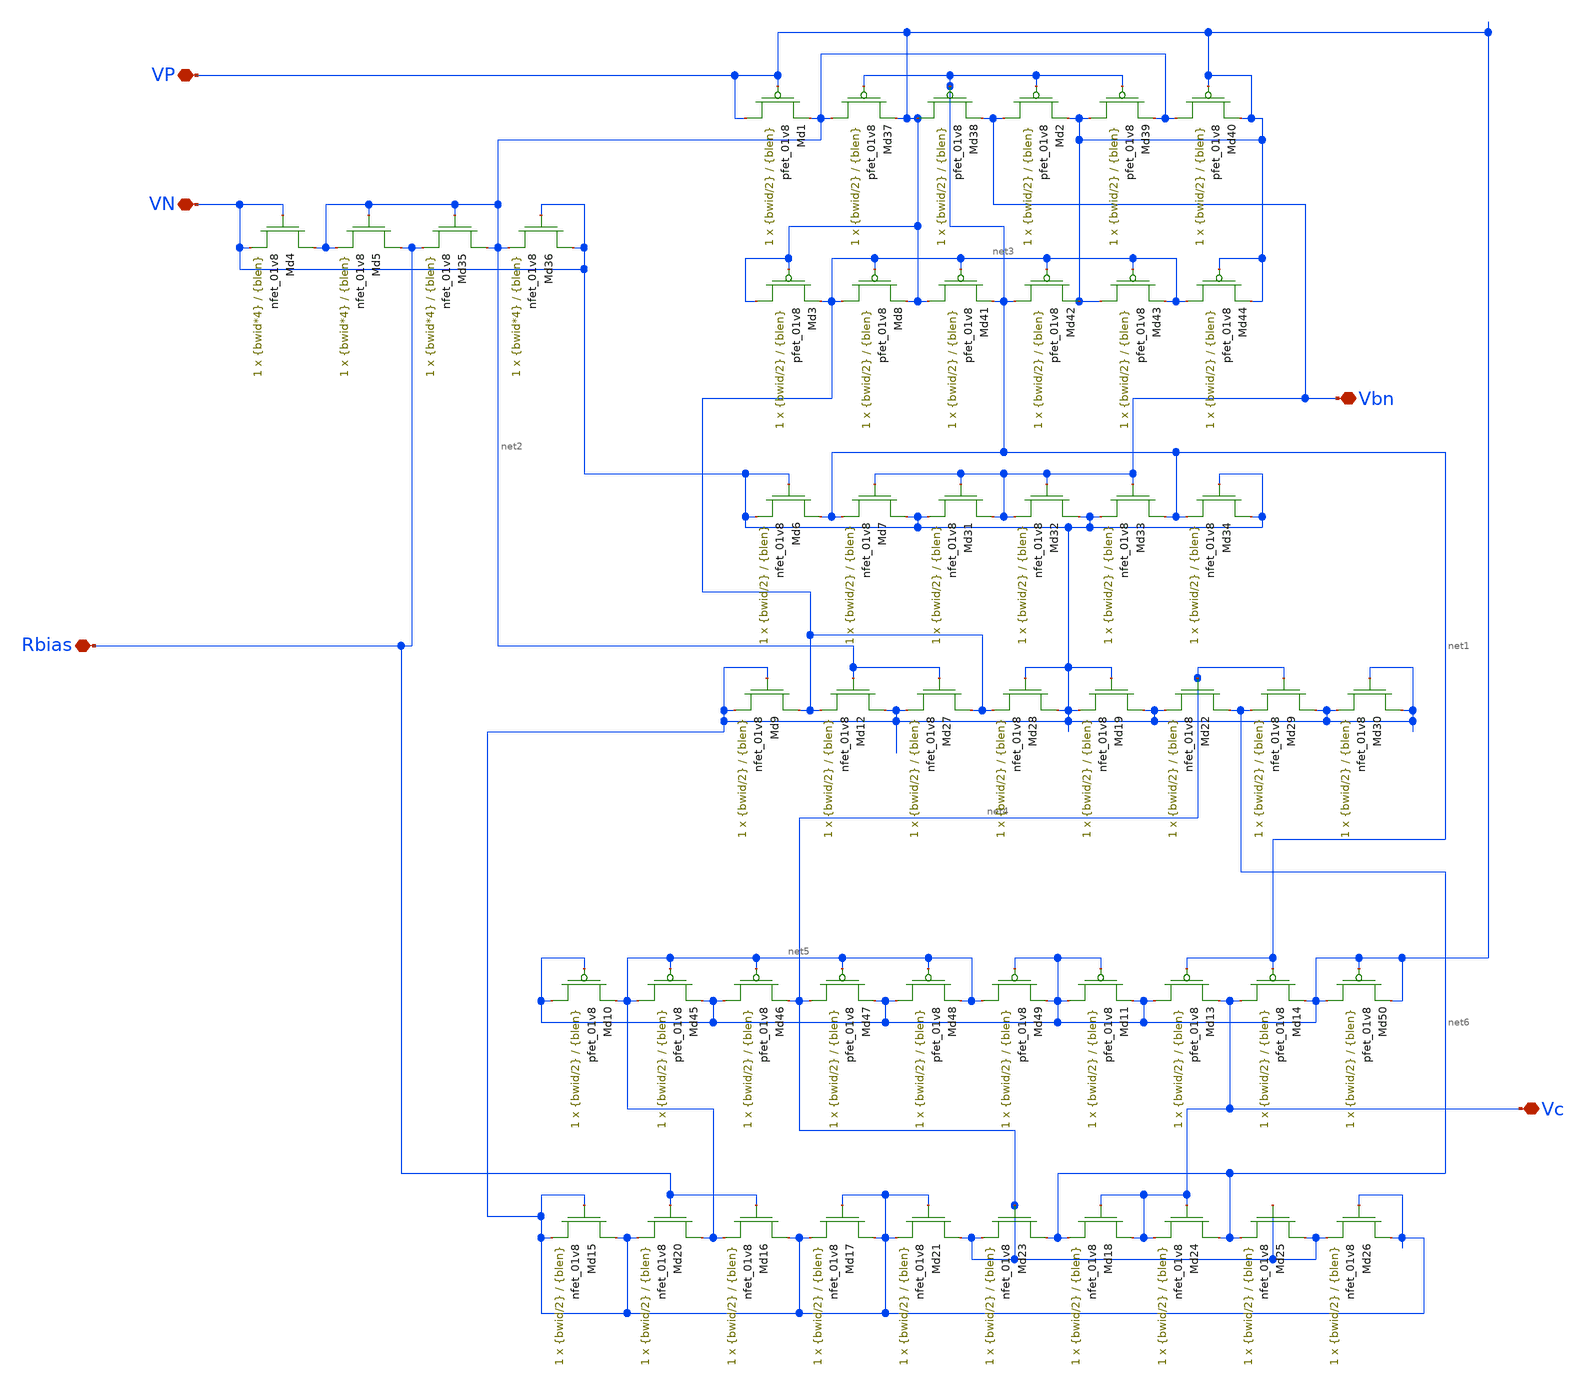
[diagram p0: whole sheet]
** sch_path: design-files/improved/biasgen-m2.sch
**.subckt biasgen-m2 Rbias Vbn Vc VP VN
*.iopin Rbias
*.iopin Vbn
*.iopin Vc
*.iopin VP
*.iopin VN
XMd1 VP VP net2 VDD sky130_fd_pr__pfet_01v8 L={blen} W={bwid/2} nf=1 ad='int((nf+1)/2) * W/nf * 0.29'
+ as='int((nf+2)/2) * W/nf * 0.29' pd='2*int((nf+1)/2) * (W/nf + 0.29)' ps='2*int((nf+2)/2) * (W/nf + 0.29)'
+ nrd='0.29 / W' nrs='0.29 / W' sa=0 sb=0 sd=0 mult=1 m=1
XMd15 VN VN VN GND sky130_fd_pr__nfet_01v8 L={blen} W={bwid/2} nf=1 ad='int((nf+1)/2) * W/nf * 0.29'
+ as='int((nf+2)/2) * W/nf * 0.29' pd='2*int((nf+1)/2) * (W/nf + 0.29)' ps='2*int((nf+2)/2) * (W/nf + 0.29)'
+ nrd='0.29 / W' nrs='0.29 / W' sa=0 sb=0 sd=0 mult=1 m=1
XMd20 net5 Rbias VN GND sky130_fd_pr__nfet_01v8 L={blen} W={bwid/2} nf=1 ad='int((nf+1)/2) * W/nf * 0.29'
+ as='int((nf+2)/2) * W/nf * 0.29' pd='2*int((nf+1)/2) * (W/nf + 0.29)' ps='2*int((nf+2)/2) * (W/nf + 0.29)'
+ nrd='0.29 / W' nrs='0.29 / W' sa=0 sb=0 sd=0 mult=1 m=1
XMd16 VN Rbias net5 GND sky130_fd_pr__nfet_01v8 L={blen} W={bwid/2} nf=1 ad='int((nf+1)/2) * W/nf * 0.29'
+ as='int((nf+2)/2) * W/nf * 0.29' pd='2*int((nf+1)/2) * (W/nf + 0.29)' ps='2*int((nf+2)/2) * (W/nf + 0.29)'
+ nrd='0.29 / W' nrs='0.29 / W' sa=0 sb=0 sd=0 mult=1 m=1
XMd17 VN VN VN GND sky130_fd_pr__nfet_01v8 L={blen} W={bwid/2} nf=1 ad='int((nf+1)/2) * W/nf * 0.29'
+ as='int((nf+2)/2) * W/nf * 0.29' pd='2*int((nf+1)/2) * (W/nf + 0.29)' ps='2*int((nf+2)/2) * (W/nf + 0.29)'
+ nrd='0.29 / W' nrs='0.29 / W' sa=0 sb=0 sd=0 mult=1 m=1
XMd21 net4 VN VN GND sky130_fd_pr__nfet_01v8 L={blen} W={bwid/2} nf=1 ad='int((nf+1)/2) * W/nf * 0.29'
+ as='int((nf+2)/2) * W/nf * 0.29' pd='2*int((nf+1)/2) * (W/nf + 0.29)' ps='2*int((nf+2)/2) * (W/nf + 0.29)'
+ nrd='0.29 / W' nrs='0.29 / W' sa=0 sb=0 sd=0 mult=1 m=1
XMd23 net6 net4 net4 GND sky130_fd_pr__nfet_01v8 L={blen} W={bwid/2} nf=1 ad='int((nf+1)/2) * W/nf * 0.29'
+ as='int((nf+2)/2) * W/nf * 0.29' pd='2*int((nf+1)/2) * (W/nf + 0.29)' ps='2*int((nf+2)/2) * (W/nf + 0.29)'
+ nrd='0.29 / W' nrs='0.29 / W' sa=0 sb=0 sd=0 mult=1 m=1
XMd18 Vc Vc net6 GND sky130_fd_pr__nfet_01v8 L={blen} W={bwid/2} nf=1 ad='int((nf+1)/2) * W/nf * 0.29'
+ as='int((nf+2)/2) * W/nf * 0.29' pd='2*int((nf+1)/2) * (W/nf + 0.29)' ps='2*int((nf+2)/2) * (W/nf + 0.29)'
+ nrd='0.29 / W' nrs='0.29 / W' sa=0 sb=0 sd=0 mult=1 m=1
XMd24 net6 Vc Vc GND sky130_fd_pr__nfet_01v8 L={blen} W={bwid/2} nf=1 ad='int((nf+1)/2) * W/nf * 0.29'
+ as='int((nf+2)/2) * W/nf * 0.29' pd='2*int((nf+1)/2) * (W/nf + 0.29)' ps='2*int((nf+2)/2) * (W/nf + 0.29)'
+ nrd='0.29 / W' nrs='0.29 / W' sa=0 sb=0 sd=0 mult=1 m=1
XMd25 net4 net4 net6 GND sky130_fd_pr__nfet_01v8 L={blen} W={bwid/2} nf=1 ad='int((nf+1)/2) * W/nf * 0.29'
+ as='int((nf+2)/2) * W/nf * 0.29' pd='2*int((nf+1)/2) * (W/nf + 0.29)' ps='2*int((nf+2)/2) * (W/nf + 0.29)'
+ nrd='0.29 / W' nrs='0.29 / W' sa=0 sb=0 sd=0 mult=1 m=1
XMd26 VN VN net4 GND sky130_fd_pr__nfet_01v8 L={blen} W={bwid/2} nf=1 ad='int((nf+1)/2) * W/nf * 0.29'
+ as='int((nf+2)/2) * W/nf * 0.29' pd='2*int((nf+1)/2) * (W/nf + 0.29)' ps='2*int((nf+2)/2) * (W/nf + 0.29)'
+ nrd='0.29 / W' nrs='0.29 / W' sa=0 sb=0 sd=0 mult=1 m=1
XMd9 net3 VN VN GND sky130_fd_pr__nfet_01v8 L={blen} W={bwid/2} nf=1 ad='int((nf+1)/2) * W/nf * 0.29'
+ as='int((nf+2)/2) * W/nf * 0.29' pd='2*int((nf+1)/2) * (W/nf + 0.29)' ps='2*int((nf+2)/2) * (W/nf + 0.29)'
+ nrd='0.29 / W' nrs='0.29 / W' sa=0 sb=0 sd=0 mult=1 m=1
XMd12 VN net2 net3 GND sky130_fd_pr__nfet_01v8 L={blen} W={bwid/2} nf=1 ad='int((nf+1)/2) * W/nf * 0.29'
+ as='int((nf+2)/2) * W/nf * 0.29' pd='2*int((nf+1)/2) * (W/nf + 0.29)' ps='2*int((nf+2)/2) * (W/nf + 0.29)'
+ nrd='0.29 / W' nrs='0.29 / W' sa=0 sb=0 sd=0 mult=1 m=1
XMd27 net3 net2 VN GND sky130_fd_pr__nfet_01v8 L={blen} W={bwid/2} nf=1 ad='int((nf+1)/2) * W/nf * 0.29'
+ as='int((nf+2)/2) * W/nf * 0.29' pd='2*int((nf+1)/2) * (W/nf + 0.29)' ps='2*int((nf+2)/2) * (W/nf + 0.29)'
+ nrd='0.29 / W' nrs='0.29 / W' sa=0 sb=0 sd=0 mult=1 m=1
XMd28 VN VN net3 GND sky130_fd_pr__nfet_01v8 L={blen} W={bwid/2} nf=1 ad='int((nf+1)/2) * W/nf * 0.29'
+ as='int((nf+2)/2) * W/nf * 0.29' pd='2*int((nf+1)/2) * (W/nf + 0.29)' ps='2*int((nf+2)/2) * (W/nf + 0.29)'
+ nrd='0.29 / W' nrs='0.29 / W' sa=0 sb=0 sd=0 mult=1 m=1
XMd19 VN VN VN GND sky130_fd_pr__nfet_01v8 L={blen} W={bwid/2} nf=1 ad='int((nf+1)/2) * W/nf * 0.29'
+ as='int((nf+2)/2) * W/nf * 0.29' pd='2*int((nf+1)/2) * (W/nf + 0.29)' ps='2*int((nf+2)/2) * (W/nf + 0.29)'
+ nrd='0.29 / W' nrs='0.29 / W' sa=0 sb=0 sd=0 mult=1 m=1
XMd22 net6 net4 VN GND sky130_fd_pr__nfet_01v8 L={blen} W={bwid/2} nf=1 ad='int((nf+1)/2) * W/nf * 0.29'
+ as='int((nf+2)/2) * W/nf * 0.29' pd='2*int((nf+1)/2) * (W/nf + 0.29)' ps='2*int((nf+2)/2) * (W/nf + 0.29)'
+ nrd='0.29 / W' nrs='0.29 / W' sa=0 sb=0 sd=0 mult=1 m=1
XMd29 VN net4 net6 GND sky130_fd_pr__nfet_01v8 L={blen} W={bwid/2} nf=1 ad='int((nf+1)/2) * W/nf * 0.29'
+ as='int((nf+2)/2) * W/nf * 0.29' pd='2*int((nf+1)/2) * (W/nf + 0.29)' ps='2*int((nf+2)/2) * (W/nf + 0.29)'
+ nrd='0.29 / W' nrs='0.29 / W' sa=0 sb=0 sd=0 mult=1 m=1
XMd30 VN VN VN GND sky130_fd_pr__nfet_01v8 L={blen} W={bwid/2} nf=1 ad='int((nf+1)/2) * W/nf * 0.29'
+ as='int((nf+2)/2) * W/nf * 0.29' pd='2*int((nf+1)/2) * (W/nf + 0.29)' ps='2*int((nf+2)/2) * (W/nf + 0.29)'
+ nrd='0.29 / W' nrs='0.29 / W' sa=0 sb=0 sd=0 mult=1 m=1
XMd6 net1 VN VN GND sky130_fd_pr__nfet_01v8 L={blen} W={bwid/2} nf=1 ad='int((nf+1)/2) * W/nf * 0.29'
+ as='int((nf+2)/2) * W/nf * 0.29' pd='2*int((nf+1)/2) * (W/nf + 0.29)' ps='2*int((nf+2)/2) * (W/nf + 0.29)'
+ nrd='0.29 / W' nrs='0.29 / W' sa=0 sb=0 sd=0 mult=1 m=1
XMd7 VN Vbn net1 GND sky130_fd_pr__nfet_01v8 L={blen} W={bwid/2} nf=1 ad='int((nf+1)/2) * W/nf * 0.29'
+ as='int((nf+2)/2) * W/nf * 0.29' pd='2*int((nf+1)/2) * (W/nf + 0.29)' ps='2*int((nf+2)/2) * (W/nf + 0.29)'
+ nrd='0.29 / W' nrs='0.29 / W' sa=0 sb=0 sd=0 mult=1 m=1
XMd31 Vbn Vbn VN GND sky130_fd_pr__nfet_01v8 L={blen} W={bwid/2} nf=1 ad='int((nf+1)/2) * W/nf * 0.29'
+ as='int((nf+2)/2) * W/nf * 0.29' pd='2*int((nf+1)/2) * (W/nf + 0.29)' ps='2*int((nf+2)/2) * (W/nf + 0.29)'
+ nrd='0.29 / W' nrs='0.29 / W' sa=0 sb=0 sd=0 mult=1 m=1
XMd32 VN Vbn Vbn GND sky130_fd_pr__nfet_01v8 L={blen} W={bwid/2} nf=1 ad='int((nf+1)/2) * W/nf * 0.29'
+ as='int((nf+2)/2) * W/nf * 0.29' pd='2*int((nf+1)/2) * (W/nf + 0.29)' ps='2*int((nf+2)/2) * (W/nf + 0.29)'
+ nrd='0.29 / W' nrs='0.29 / W' sa=0 sb=0 sd=0 mult=1 m=1
XMd33 net1 Vbn VN GND sky130_fd_pr__nfet_01v8 L={blen} W={bwid/2} nf=1 ad='int((nf+1)/2) * W/nf * 0.29'
+ as='int((nf+2)/2) * W/nf * 0.29' pd='2*int((nf+1)/2) * (W/nf + 0.29)' ps='2*int((nf+2)/2) * (W/nf + 0.29)'
+ nrd='0.29 / W' nrs='0.29 / W' sa=0 sb=0 sd=0 mult=1 m=1
XMd34 VN VN net1 GND sky130_fd_pr__nfet_01v8 L={blen} W={bwid/2} nf=1 ad='int((nf+1)/2) * W/nf * 0.29'
+ as='int((nf+2)/2) * W/nf * 0.29' pd='2*int((nf+1)/2) * (W/nf + 0.29)' ps='2*int((nf+2)/2) * (W/nf + 0.29)'
+ nrd='0.29 / W' nrs='0.29 / W' sa=0 sb=0 sd=0 mult=1 m=1
XMd4 net2 VN VN GND sky130_fd_pr__nfet_01v8 L={blen} W={bwid*4} nf=1 ad='int((nf+1)/2) * W/nf * 0.29'
+ as='int((nf+2)/2) * W/nf * 0.29' pd='2*int((nf+1)/2) * (W/nf + 0.29)' ps='2*int((nf+2)/2) * (W/nf + 0.29)'
+ nrd='0.29 / W' nrs='0.29 / W' sa=0 sb=0 sd=0 mult=1 m=1
XMd5 Rbias net2 net2 GND sky130_fd_pr__nfet_01v8 L={blen} W={bwid*4} nf=1 ad='int((nf+1)/2) * W/nf * 0.29'
+ as='int((nf+2)/2) * W/nf * 0.29' pd='2*int((nf+1)/2) * (W/nf + 0.29)' ps='2*int((nf+2)/2) * (W/nf + 0.29)'
+ nrd='0.29 / W' nrs='0.29 / W' sa=0 sb=0 sd=0 mult=1 m=1
XMd35 net2 net2 Rbias GND sky130_fd_pr__nfet_01v8 L={blen} W={bwid*4} nf=1 ad='int((nf+1)/2) * W/nf * 0.29'
+ as='int((nf+2)/2) * W/nf * 0.29' pd='2*int((nf+1)/2) * (W/nf + 0.29)' ps='2*int((nf+2)/2) * (W/nf + 0.29)'
+ nrd='0.29 / W' nrs='0.29 / W' sa=0 sb=0 sd=0 mult=1 m=1
XMd36 VN VN net2 GND sky130_fd_pr__nfet_01v8 L={blen} W={bwid*4} nf=1 ad='int((nf+1)/2) * W/nf * 0.29'
+ as='int((nf+2)/2) * W/nf * 0.29' pd='2*int((nf+1)/2) * (W/nf + 0.29)' ps='2*int((nf+2)/2) * (W/nf + 0.29)'
+ nrd='0.29 / W' nrs='0.29 / W' sa=0 sb=0 sd=0 mult=1 m=1
XMd37 net2 net1 VP VDD sky130_fd_pr__pfet_01v8 L={blen} W={bwid/2} nf=1 ad='int((nf+1)/2) * W/nf * 0.29'
+ as='int((nf+2)/2) * W/nf * 0.29' pd='2*int((nf+1)/2) * (W/nf + 0.29)' ps='2*int((nf+2)/2) * (W/nf + 0.29)'
+ nrd='0.29 / W' nrs='0.29 / W' sa=0 sb=0 sd=0 mult=1 m=1
XMd38 VP net1 Vbn VDD sky130_fd_pr__pfet_01v8 L={blen} W={bwid/2} nf=1 ad='int((nf+1)/2) * W/nf * 0.29'
+ as='int((nf+2)/2) * W/nf * 0.29' pd='2*int((nf+1)/2) * (W/nf + 0.29)' ps='2*int((nf+2)/2) * (W/nf + 0.29)'
+ nrd='0.29 / W' nrs='0.29 / W' sa=0 sb=0 sd=0 mult=1 m=1
XMd2 Vbn net1 VP VDD sky130_fd_pr__pfet_01v8 L={blen} W={bwid/2} nf=1 ad='int((nf+1)/2) * W/nf * 0.29'
+ as='int((nf+2)/2) * W/nf * 0.29' pd='2*int((nf+1)/2) * (W/nf + 0.29)' ps='2*int((nf+2)/2) * (W/nf + 0.29)'
+ nrd='0.29 / W' nrs='0.29 / W' sa=0 sb=0 sd=0 mult=1 m=1
XMd39 VP net1 net2 VDD sky130_fd_pr__pfet_01v8 L={blen} W={bwid/2} nf=1 ad='int((nf+1)/2) * W/nf * 0.29'
+ as='int((nf+2)/2) * W/nf * 0.29' pd='2*int((nf+1)/2) * (W/nf + 0.29)' ps='2*int((nf+2)/2) * (W/nf + 0.29)'
+ nrd='0.29 / W' nrs='0.29 / W' sa=0 sb=0 sd=0 mult=1 m=1
XMd40 net2 VP VP VDD sky130_fd_pr__pfet_01v8 L={blen} W={bwid/2} nf=1 ad='int((nf+1)/2) * W/nf * 0.29'
+ as='int((nf+2)/2) * W/nf * 0.29' pd='2*int((nf+1)/2) * (W/nf + 0.29)' ps='2*int((nf+2)/2) * (W/nf + 0.29)'
+ nrd='0.29 / W' nrs='0.29 / W' sa=0 sb=0 sd=0 mult=1 m=1
XMd3 VP VP net3 VDD sky130_fd_pr__pfet_01v8 L={blen} W={bwid/2} nf=1 ad='int((nf+1)/2) * W/nf * 0.29'
+ as='int((nf+2)/2) * W/nf * 0.29' pd='2*int((nf+1)/2) * (W/nf + 0.29)' ps='2*int((nf+2)/2) * (W/nf + 0.29)'
+ nrd='0.29 / W' nrs='0.29 / W' sa=0 sb=0 sd=0 mult=1 m=1
XMd8 net3 net3 VP VDD sky130_fd_pr__pfet_01v8 L={blen} W={bwid/2} nf=1 ad='int((nf+1)/2) * W/nf * 0.29'
+ as='int((nf+2)/2) * W/nf * 0.29' pd='2*int((nf+1)/2) * (W/nf + 0.29)' ps='2*int((nf+2)/2) * (W/nf + 0.29)'
+ nrd='0.29 / W' nrs='0.29 / W' sa=0 sb=0 sd=0 mult=1 m=1
XMd41 VP net3 net1 VDD sky130_fd_pr__pfet_01v8 L={blen} W={bwid/2} nf=1 ad='int((nf+1)/2) * W/nf * 0.29'
+ as='int((nf+2)/2) * W/nf * 0.29' pd='2*int((nf+1)/2) * (W/nf + 0.29)' ps='2*int((nf+2)/2) * (W/nf + 0.29)'
+ nrd='0.29 / W' nrs='0.29 / W' sa=0 sb=0 sd=0 mult=1 m=1
XMd42 net1 net3 VP VDD sky130_fd_pr__pfet_01v8 L={blen} W={bwid/2} nf=1 ad='int((nf+1)/2) * W/nf * 0.29'
+ as='int((nf+2)/2) * W/nf * 0.29' pd='2*int((nf+1)/2) * (W/nf + 0.29)' ps='2*int((nf+2)/2) * (W/nf + 0.29)'
+ nrd='0.29 / W' nrs='0.29 / W' sa=0 sb=0 sd=0 mult=1 m=1
XMd43 VP net3 net3 VDD sky130_fd_pr__pfet_01v8 L={blen} W={bwid/2} nf=1 ad='int((nf+1)/2) * W/nf * 0.29'
+ as='int((nf+2)/2) * W/nf * 0.29' pd='2*int((nf+1)/2) * (W/nf + 0.29)' ps='2*int((nf+2)/2) * (W/nf + 0.29)'
+ nrd='0.29 / W' nrs='0.29 / W' sa=0 sb=0 sd=0 mult=1 m=1
XMd44 net3 VP VP VDD sky130_fd_pr__pfet_01v8 L={blen} W={bwid/2} nf=1 ad='int((nf+1)/2) * W/nf * 0.29'
+ as='int((nf+2)/2) * W/nf * 0.29' pd='2*int((nf+1)/2) * (W/nf + 0.29)' ps='2*int((nf+2)/2) * (W/nf + 0.29)'
+ nrd='0.29 / W' nrs='0.29 / W' sa=0 sb=0 sd=0 mult=1 m=1
XMd10 VP VP net5 VDD sky130_fd_pr__pfet_01v8 L={blen} W={bwid/2} nf=1 ad='int((nf+1)/2) * W/nf * 0.29'
+ as='int((nf+2)/2) * W/nf * 0.29' pd='2*int((nf+1)/2) * (W/nf + 0.29)' ps='2*int((nf+2)/2) * (W/nf + 0.29)'
+ nrd='0.29 / W' nrs='0.29 / W' sa=0 sb=0 sd=0 mult=1 m=1
XMd45 net5 net5 VP VDD sky130_fd_pr__pfet_01v8 L={blen} W={bwid/2} nf=1 ad='int((nf+1)/2) * W/nf * 0.29'
+ as='int((nf+2)/2) * W/nf * 0.29' pd='2*int((nf+1)/2) * (W/nf + 0.29)' ps='2*int((nf+2)/2) * (W/nf + 0.29)'
+ nrd='0.29 / W' nrs='0.29 / W' sa=0 sb=0 sd=0 mult=1 m=1
XMd46 VP net5 net4 VDD sky130_fd_pr__pfet_01v8 L={blen} W={bwid/2} nf=1 ad='int((nf+1)/2) * W/nf * 0.29'
+ as='int((nf+2)/2) * W/nf * 0.29' pd='2*int((nf+1)/2) * (W/nf + 0.29)' ps='2*int((nf+2)/2) * (W/nf + 0.29)'
+ nrd='0.29 / W' nrs='0.29 / W' sa=0 sb=0 sd=0 mult=1 m=1
XMd47 net4 net5 VP VDD sky130_fd_pr__pfet_01v8 L={blen} W={bwid/2} nf=1 ad='int((nf+1)/2) * W/nf * 0.29'
+ as='int((nf+2)/2) * W/nf * 0.29' pd='2*int((nf+1)/2) * (W/nf + 0.29)' ps='2*int((nf+2)/2) * (W/nf + 0.29)'
+ nrd='0.29 / W' nrs='0.29 / W' sa=0 sb=0 sd=0 mult=1 m=1
XMd48 VP net5 net5 VDD sky130_fd_pr__pfet_01v8 L={blen} W={bwid/2} nf=1 ad='int((nf+1)/2) * W/nf * 0.29'
+ as='int((nf+2)/2) * W/nf * 0.29' pd='2*int((nf+1)/2) * (W/nf + 0.29)' ps='2*int((nf+2)/2) * (W/nf + 0.29)'
+ nrd='0.29 / W' nrs='0.29 / W' sa=0 sb=0 sd=0 mult=1 m=1
XMd49 net5 VP VP VDD sky130_fd_pr__pfet_01v8 L={blen} W={bwid/2} nf=1 ad='int((nf+1)/2) * W/nf * 0.29'
+ as='int((nf+2)/2) * W/nf * 0.29' pd='2*int((nf+1)/2) * (W/nf + 0.29)' ps='2*int((nf+2)/2) * (W/nf + 0.29)'
+ nrd='0.29 / W' nrs='0.29 / W' sa=0 sb=0 sd=0 mult=1 m=1
XMd11 VP VP VP VDD sky130_fd_pr__pfet_01v8 L={blen} W={bwid/2} nf=1 ad='int((nf+1)/2) * W/nf * 0.29'
+ as='int((nf+2)/2) * W/nf * 0.29' pd='2*int((nf+1)/2) * (W/nf + 0.29)' ps='2*int((nf+2)/2) * (W/nf + 0.29)'
+ nrd='0.29 / W' nrs='0.29 / W' sa=0 sb=0 sd=0 mult=1 m=1
XMd13 VP net1 Vc VDD sky130_fd_pr__pfet_01v8 L={blen} W={bwid/2} nf=1 ad='int((nf+1)/2) * W/nf * 0.29'
+ as='int((nf+2)/2) * W/nf * 0.29' pd='2*int((nf+1)/2) * (W/nf + 0.29)' ps='2*int((nf+2)/2) * (W/nf + 0.29)'
+ nrd='0.29 / W' nrs='0.29 / W' sa=0 sb=0 sd=0 mult=1 m=1
XMd14 Vc net1 VP VDD sky130_fd_pr__pfet_01v8 L={blen} W={bwid/2} nf=1 ad='int((nf+1)/2) * W/nf * 0.29'
+ as='int((nf+2)/2) * W/nf * 0.29' pd='2*int((nf+1)/2) * (W/nf + 0.29)' ps='2*int((nf+2)/2) * (W/nf + 0.29)'
+ nrd='0.29 / W' nrs='0.29 / W' sa=0 sb=0 sd=0 mult=1 m=1
XMd50 VP VP VP VDD sky130_fd_pr__pfet_01v8 L={blen} W={bwid/2} nf=1 ad='int((nf+1)/2) * W/nf * 0.29'
+ as='int((nf+2)/2) * W/nf * 0.29' pd='2*int((nf+1)/2) * (W/nf + 0.29)' ps='2*int((nf+2)/2) * (W/nf + 0.29)'
+ nrd='0.29 / W' nrs='0.29 / W' sa=0 sb=0 sd=0 mult=1 m=1
**.ends
.end
